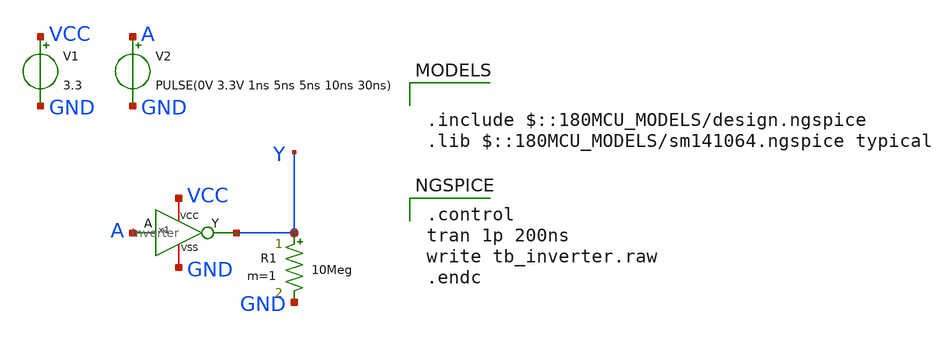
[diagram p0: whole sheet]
** sch_path: xschem/tb_inverter.sch
**.subckt tb_inverter
x1 VCC GND Y A inverter
V1 VCC GND 3.3
R1 Y GND 10Meg m=1
V2 A GND PULSE(0V 3.3V 1ns 5ns 5ns 10ns 30ns)
**** begin user architecture code

.include $::180MCU_MODELS/design.ngspice
.lib $::180MCU_MODELS/sm141064.ngspice typical


.control
tran 1p 200ns
write tb_inverter.raw
.endc

**** end user architecture code
**.ends

* expanding   symbol:  inverter.sym # of pins=4
** sym_path: xschem/inverter.sym
** sch_path: xschem/inverter.sch
.subckt inverter VCC VSS Y A
*.iopin VCC
*.iopin VSS
*.ipin A
*.opin Y
XM1 Y A VSS VSS nfet_03v3 L=0.50u W=0.25u nf=1 ad='int((nf+1)/2) * W/nf * 0.18u' as='int((nf+2)/2) * W/nf * 0.18u'
+ pd='2*int((nf+1)/2) * (W/nf + 0.18u)' ps='2*int((nf+2)/2) * (W/nf + 0.18u)' nrd='0.18u / W' nrs='0.18u / W'
+ sa=0 sb=0 sd=0 m=1
XM2 Y A VCC VCC pfet_03v3 L=0.50u W=0.50u nf=1 ad='int((nf+1)/2) * W/nf * 0.18u' as='int((nf+2)/2) * W/nf * 0.18u'
+ pd='2*int((nf+1)/2) * (W/nf + 0.18u)' ps='2*int((nf+2)/2) * (W/nf + 0.18u)' nrd='0.18u / W' nrs='0.18u / W'
+ sa=0 sb=0 sd=0 m=1
.ends

.end
